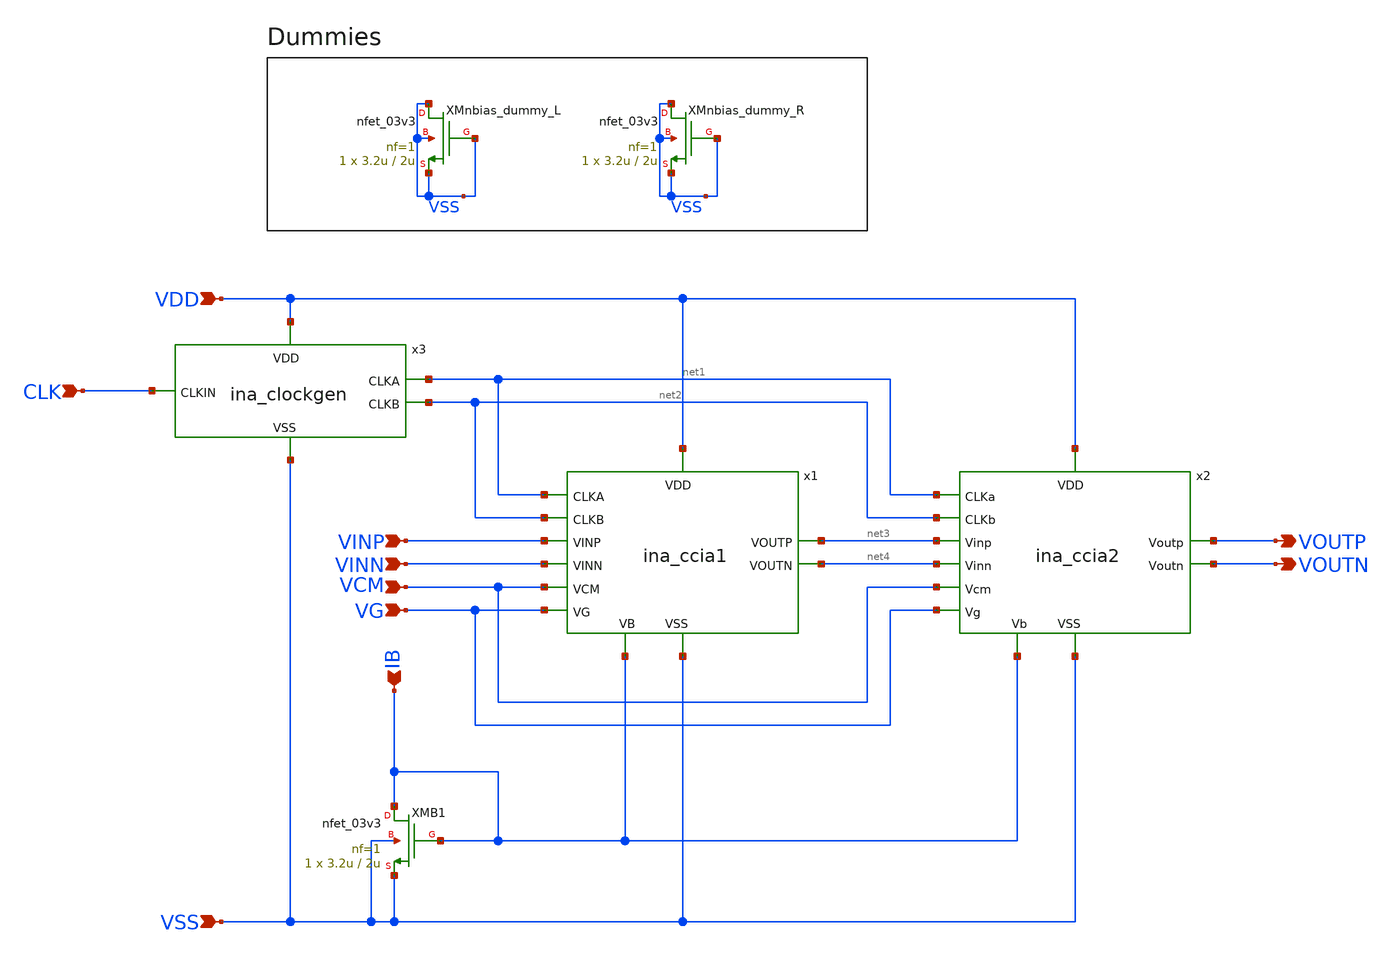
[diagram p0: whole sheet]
** sch_path: designs/libs/core_ina/ina/ina.sch
**.subckt ina CLK VINP VINN VDD VSS VCM IB VG VOUTP VOUTN
*.ipin CLK
*.ipin VINP
*.ipin VINN
*.ipin VDD
*.ipin VSS
*.ipin VCM
*.ipin IB
*.ipin VG
*.opin VOUTP
*.opin VOUTN
x3 VDD CLK net1 net2 VSS ina_clockgen
XMB1 IB IB VSS VSS nfet_03v3 L=2u W=3.2u nf=1 ad='int((nf+1)/2) * W/nf * 0.18u' as='int((nf+2)/2) * W/nf * 0.18u'
+ pd='2*int((nf+1)/2) * (W/nf + 0.18u)' ps='2*int((nf+2)/2) * (W/nf + 0.18u)' nrd='0.18u / W' nrs='0.18u / W'
+ sa=0 sb=0 sd=0 m=1
XMnbias_dummy_L VSS VSS VSS VSS nfet_03v3 L=2u W=3.2u nf=1 ad='int((nf+1)/2) * W/nf * 0.18u' as='int((nf+2)/2) * W/nf * 0.18u'
+ pd='2*int((nf+1)/2) * (W/nf + 0.18u)' ps='2*int((nf+2)/2) * (W/nf + 0.18u)' nrd='0.18u / W' nrs='0.18u / W'
+ sa=0 sb=0 sd=0 m=1
XMnbias_dummy_R VSS VSS VSS VSS nfet_03v3 L=2u W=3.2u nf=1 ad='int((nf+1)/2) * W/nf * 0.18u' as='int((nf+2)/2) * W/nf * 0.18u'
+ pd='2*int((nf+1)/2) * (W/nf + 0.18u)' ps='2*int((nf+2)/2) * (W/nf + 0.18u)' nrd='0.18u / W' nrs='0.18u / W'
+ sa=0 sb=0 sd=0 m=1
x1 VG VINP VDD net3 VINN net4 net1 net2 VCM IB VSS ina_ccia1
x2 VG net3 VDD VOUTP net4 VOUTN net1 net2 VCM IB VSS ina_ccia2
**.ends
.end
